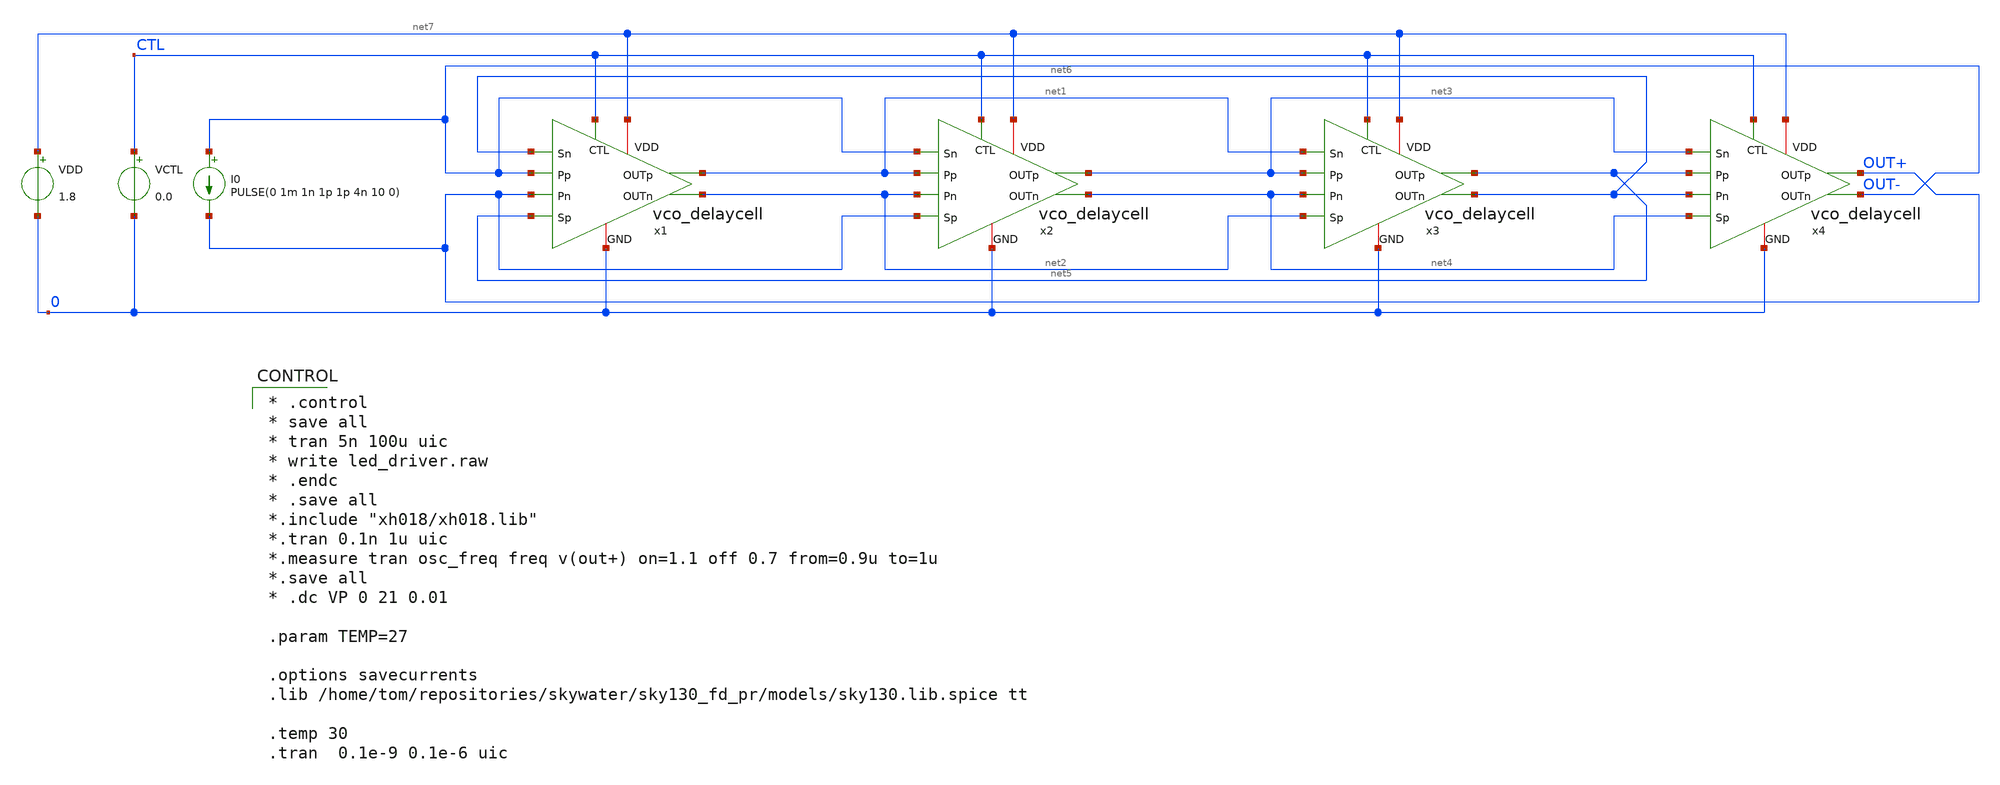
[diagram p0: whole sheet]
** sch_path: design/vco_delaycell_feedforward/tests/vco_delaycell_tb.sch
**.subckt vco_delaycell_tb
x1 net7 net5 net6 net2 net1 OUT+ OUT- 0 CTL vco_delaycell sec_w=sec_w load_w=load_w ctl_w=ctl_w
+ prim_w=prim_w cross_w=cross_w
VDD net7 0 1.8
VCTL CTL 0 0.0
x2 net7 OUT+ OUT- net4 net3 net2 net1 0 CTL vco_delaycell sec_w=sec_w load_w=load_w ctl_w=ctl_w
+ prim_w=prim_w cross_w=cross_w
x3 net7 net2 net1 net6 net5 net4 net3 0 CTL vco_delaycell sec_w=sec_w load_w=load_w ctl_w=ctl_w
+ prim_w=prim_w cross_w=cross_w
x4 net7 net4 net3 OUT- OUT+ net6 net5 0 CTL vco_delaycell sec_w=sec_w load_w=load_w ctl_w=ctl_w
+ prim_w=prim_w cross_w=cross_w
I0 OUT- OUT+ PULSE(0 1m 1n 1p 1p 4n 10 0)
**** begin user architecture code

* .control
* save all
* tran 5n 100u uic
* write led_driver.raw
* .endc
* .save all
*.include "xh018/xh018.lib"
*.tran 0.1n 1u uic
*.measure tran osc_freq freq v(out+) on=1.1 off 0.7 from=0.9u to=1u
*.save all
* .dc VP 0 21 0.01

.param TEMP=27

.options savecurrents
.lib /home/tom/repositories/skywater/sky130_fd_pr/models/sky130.lib.spice tt

.temp 30
.tran  0.1e-9 0.1e-6 uic


**** end user architecture code
**.ends

* expanding   symbol:  vco_delaycell/vco_delaycell.sym # of pins=9
** sym_path: design/vco_delaycell_feedforward/vco_delaycell.sym
** sch_path: design/vco_delaycell_feedforward/vco_delaycell.sch
.subckt vco_delaycell VDD Sp Sn OUTn OUTp Pn Pp GND CTL  sec_w=100u load_w=0.22u ctl_w=100u
+ prim_w=200u cross_w=0.22u
*.ipin Pp
*.ipin Pn
*.ipin Sp
*.ipin Sn
*.opin OUTn
*.opin OUTp
*.iopin VDD
*.iopin GND
*.ipin CTL
XMprimpos OUTp Pp GND GND sky130_fd_pr__rf_nfet_01v8_bM04W5p00L0p15 w=5u l=0.18u m=1
XMcrossneg OUTn OUTp GND GND sky130_fd_pr__rf_nfet_01v8_bM04W5p00L0p15 w=5u l=0.18u m=1
XMctlneg OUTn CTL VDD VDD sky130_fd_pr__rf_pfet_01v8_bM02W1p65L0p25 w=5u l=0.18u m=1
XMctlpos OUTp CTL VDD VDD sky130_fd_pr__rf_pfet_01v8_bM02W1p65L0p25 w=5u l=0.18u m=1
XMloadpos OUTp GND VDD VDD sky130_fd_pr__rf_pfet_01v8_bM02W1p65L0p25 w=5u l=0.18u m=1
XMsecdneg OUTn Sn VDD VDD sky130_fd_pr__rf_pfet_01v8_aF02W0p84L0p15 w=5u l=0.18u m=1
XMsecdpos OUTp Sp VDD VDD sky130_fd_pr__rf_pfet_01v8_aF02W0p84L0p15 w=5u l=0.18u m=1
XMcrosspos OUTp OUTn GND GND sky130_fd_pr__rf_nfet_01v8_bM04W5p00L0p15 w=5u l=0.18u m=1
XMprimneg OUTn Pn GND GND sky130_fd_pr__rf_nfet_01v8_bM04W5p00L0p15 w=5u l=0.18u m=1
XMoadneg OUTn GND VDD VDD sky130_fd_pr__rf_pfet_01v8_bM02W1p65L0p25 w=5u l=0.18u m=1
.ends

.end
